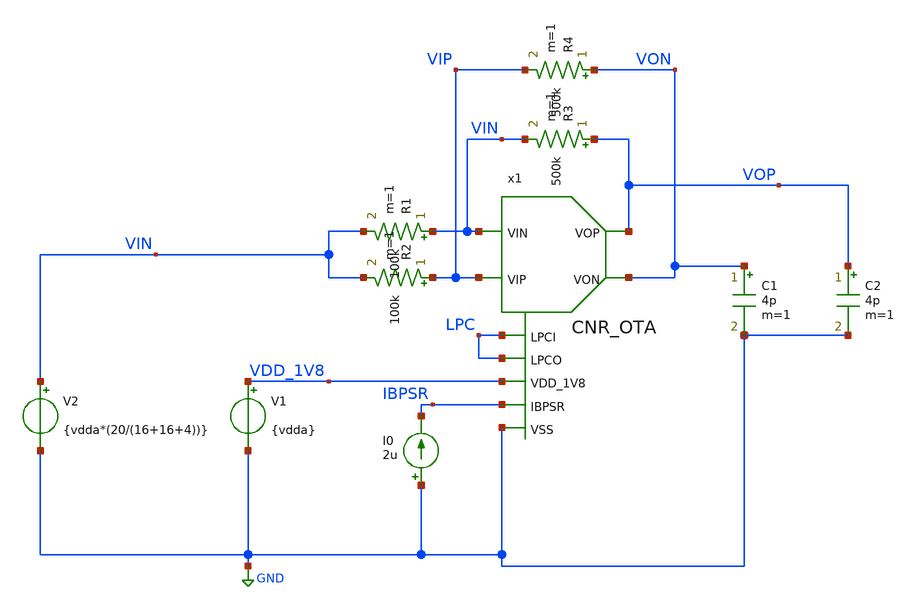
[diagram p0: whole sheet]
** sch_path: design/TB_CNR_OTA/TB_CNROTA_OP.sch
**.subckt TB_CNROTA_OP
x1 VDD_1V8 VOP VON VIN VIP IBPSR GND LPC LPC CNR_OTA
V1 VDD_1V8 GND {vdda}
I0 GND IBPSR 2u
C1 VON GND 4p m=1
C2 VOP GND 4p m=1
R1 VIN VIN 100k m=1
R2 VIP VIN 100k m=1
V2 VIN GND {vdda*(20/(16+16+4))}
R3 VOP VIN 500k m=1
R4 VON VIP 500k m=1
**** begin user architecture code



* ngspice commands
.include corner.spi



**** end user architecture code
**.ends
.GLOBAL GND
.end
